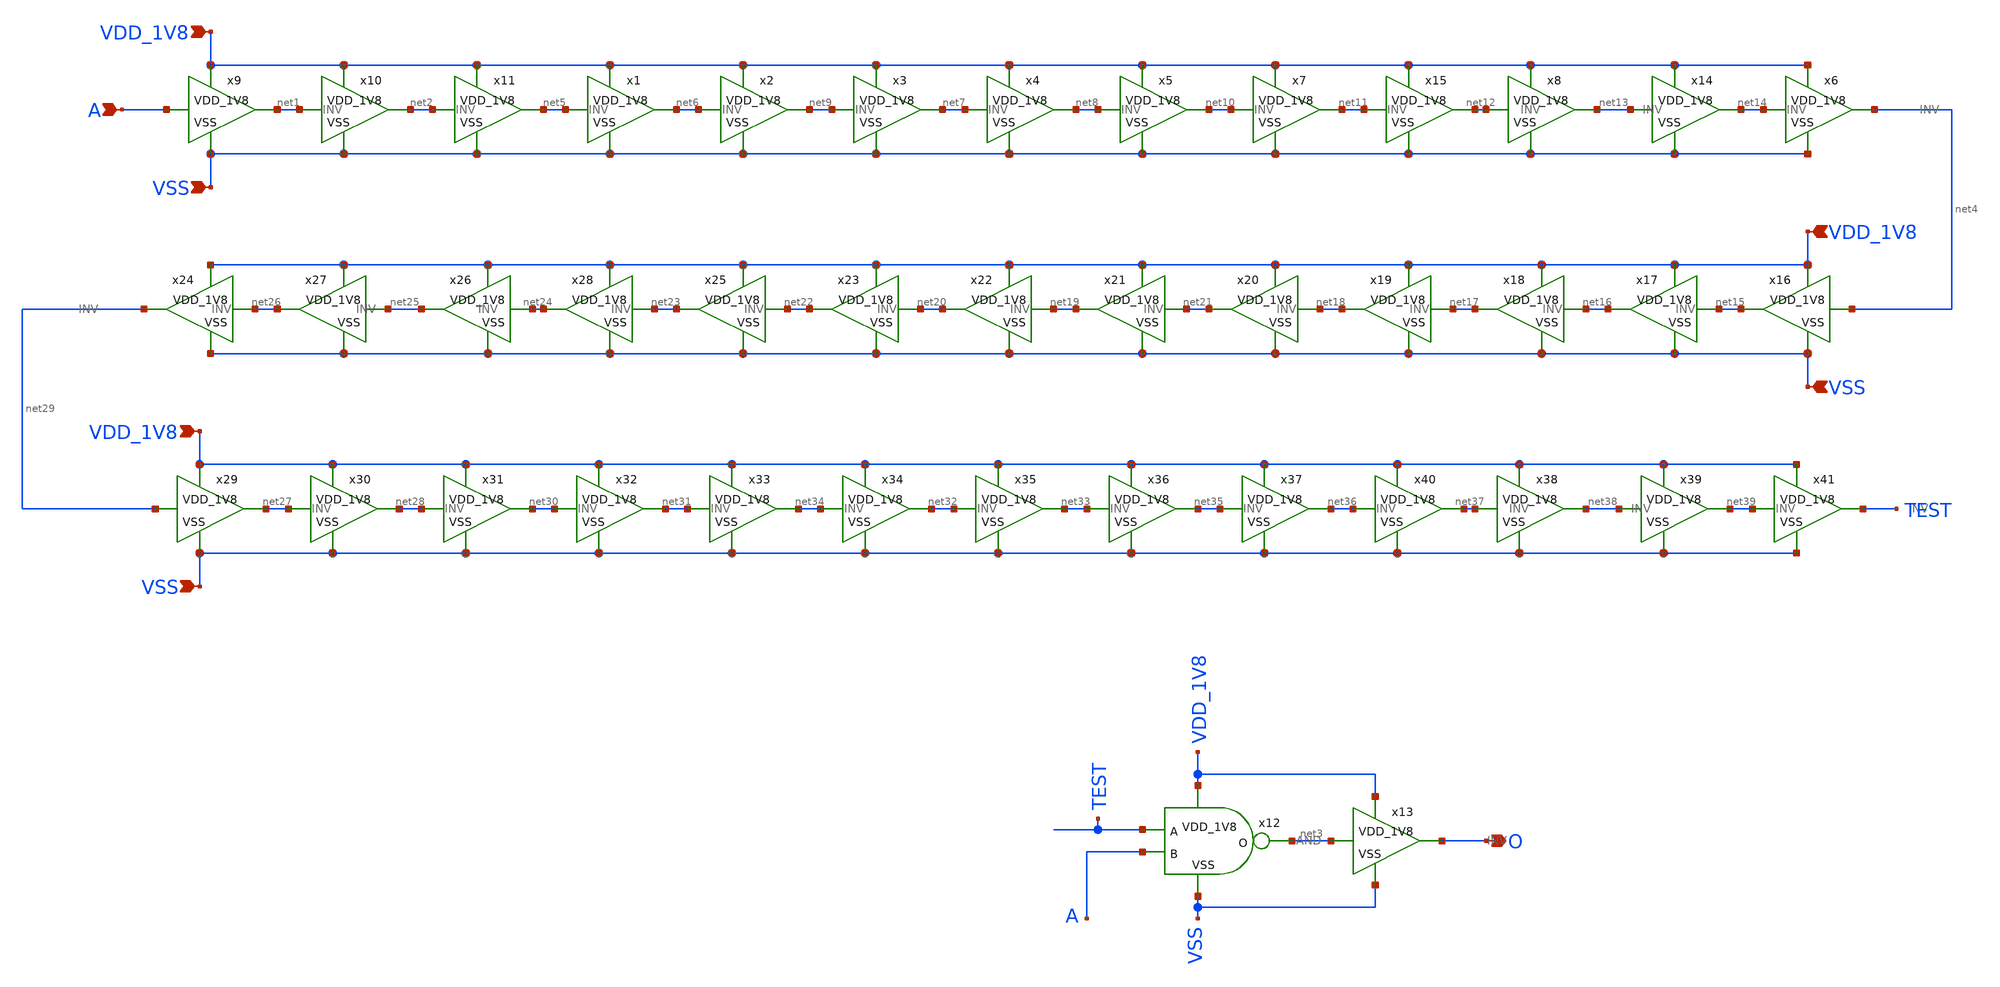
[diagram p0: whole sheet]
** sch_path: design/CNR_GR05_SKY130NM/POSEDGE.sch
**.subckt POSEDGE VDD_1V8 VSS O A VDD_1V8 VSS VDD_1V8 VSS
*.ipin VDD_1V8
*.ipin VSS
*.opin O
*.ipin A
*.ipin VDD_1V8
*.ipin VSS
*.ipin VDD_1V8
*.ipin VSS
x9 VDD_1V8 A net1 VSS INV
x10 VDD_1V8 net1 net2 VSS INV
x11 VDD_1V8 net2 net5 VSS INV
x12 VDD_1V8 TEST A net3 VSS AND
x13 VDD_1V8 net3 O VSS INV
x1 VDD_1V8 net5 net6 VSS INV
x2 VDD_1V8 net6 net9 VSS INV
x3 VDD_1V8 net9 net7 VSS INV
x4 VDD_1V8 net7 net8 VSS INV
x5 VDD_1V8 net8 net10 VSS INV
x6 VDD_1V8 net14 net4 VSS INV
x7 VDD_1V8 net10 net11 VSS INV
x8 VDD_1V8 net12 net13 VSS INV
x14 VDD_1V8 net13 net14 VSS INV
x15 VDD_1V8 net11 net12 VSS INV
x16 VDD_1V8 net4 net15 VSS INV
x17 VDD_1V8 net15 net16 VSS INV
x18 VDD_1V8 net16 net17 VSS INV
x19 VDD_1V8 net17 net18 VSS INV
x20 VDD_1V8 net18 net21 VSS INV
x21 VDD_1V8 net21 net19 VSS INV
x22 VDD_1V8 net19 net20 VSS INV
x23 VDD_1V8 net20 net22 VSS INV
x25 VDD_1V8 net22 net23 VSS INV
x26 VDD_1V8 net24 net25 VSS INV
x27 VDD_1V8 net25 net26 VSS INV
x28 VDD_1V8 net23 net24 VSS INV
x24 VDD_1V8 net26 net29 VSS INV
x29 VDD_1V8 net29 net27 VSS INV
x30 VDD_1V8 net27 net28 VSS INV
x31 VDD_1V8 net28 net30 VSS INV
x32 VDD_1V8 net30 net31 VSS INV
x33 VDD_1V8 net31 net34 VSS INV
x34 VDD_1V8 net34 net32 VSS INV
x35 VDD_1V8 net32 net33 VSS INV
x36 VDD_1V8 net33 net35 VSS INV
x37 VDD_1V8 net35 net36 VSS INV
x38 VDD_1V8 net37 net38 VSS INV
x39 VDD_1V8 net38 net39 VSS INV
x40 VDD_1V8 net36 net37 VSS INV
x41 VDD_1V8 net39 TEST VSS INV
**.ends
.end
